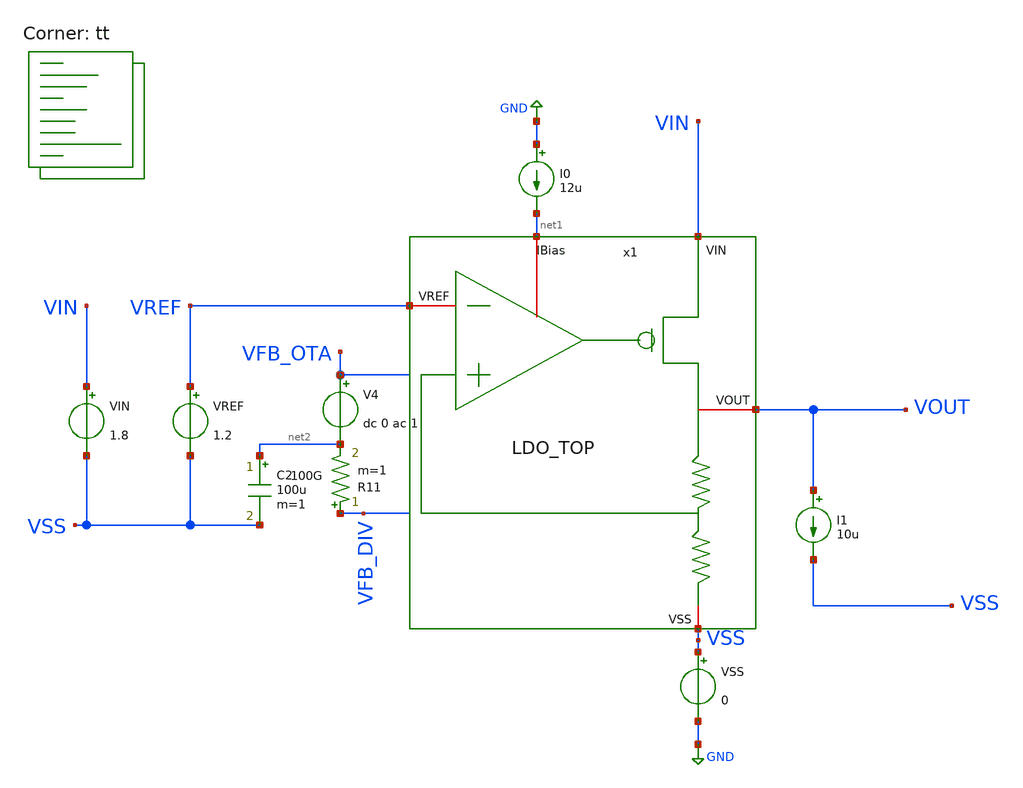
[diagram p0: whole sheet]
** sch_path: LDO_1p5V/tests/stb.sch
**.subckt stb
VSS VSS GND 0
VREF VREF VSS 1.2
VIN VIN VSS 1.8
I0 GND net1 12u
I1 VOUT VSS 10u
V4 VFB_OTA net2 dc 0 ac 1
R11 VFB_DIV net2 100G m=1
C2 net2 VSS 100u m=1
x1 VIN net1 VREF VOUT VSS LDO_TOP
**** begin user architecture code


.options savecurrents
.save all

.control
set filetype=ascii

echo ==============================================
echo ===== LDO STABILITY / LOOP GAIN ANALYSIS =====
echo ==============================================

****************************************************
* CASE 1: ILOAD = 10uA
****************************************************

echo ===== CASE 1: ILOAD = 10uA =====

alter I1 10u

op

echo ===== OPERATING POINT - ILOAD = 10uA =====
print v(VIN)
print v(VOUT)
print v(VREF)
print v(VFB_OTA)
print v(VFB_DIV)
print v(VSS)

echo ===== AC ANALYSIS - ILOAD = 10uA =====
ac dec 200 1 10g

echo ===== LOOP GAIN - ILOAD = 10uA =====

* Fuente de prueba V4: dc 0 ac 1
* La fuente está entre VFB_OTA y VFB_DIV
* La señal de retorno se mide en VFB_DIV

let loopgain_10u = -v(VFB_DIV)
let loopgain_10u_db = db(loopgain_10u)
let loopgain_10u_phase_deg = ph(loopgain_10u)*180/3.141592653589793

meas ac loop_gain_dc_10u find loopgain_10u_db at=1
meas ac unity_freq_10u when loopgain_10u_db=0
meas ac phase_at_unity_10u find loopgain_10u_phase_deg when loopgain_10u_db=0

let phase_margin_10u = 180 + phase_at_unity_10u

echo ===== RESULTS - ILOAD = 10uA =====
print loop_gain_dc_10u
print unity_freq_10u
print phase_at_unity_10u
print phase_margin_10u


****************************************************
* CASE 2: ILOAD = 1mA
****************************************************

echo ===== CASE 2: ILOAD = 1mA =====

alter I1 1m

op

echo ===== OPERATING POINT - ILOAD = 1mA =====
print v(VIN)
print v(VOUT)
print v(VREF)
print v(VFB_OTA)
print v(VFB_DIV)
print v(VSS)

echo ===== AC ANALYSIS - ILOAD = 1mA =====
ac dec 200 1 10g

echo ===== LOOP GAIN - ILOAD = 1mA =====

let loopgain_1m = -v(VFB_DIV)
let loopgain_1m_db = db(loopgain_1m)
let loopgain_1m_phase_deg = ph(loopgain_1m)*180/3.141592653589793

meas ac loop_gain_dc_1m find loopgain_1m_db at=1
meas ac unity_freq_1m when loopgain_1m_db=0
meas ac phase_at_unity_1m find loopgain_1m_phase_deg when loopgain_1m_db=0

let phase_margin_1m = 180 + phase_at_unity_1m

echo ===== RESULTS - ILOAD = 1mA =====
print loop_gain_dc_1m
print unity_freq_1m
print phase_at_unity_1m
print phase_margin_1m


****************************************************
* PLOTS - BOTH LOAD CONDITIONS
****************************************************

echo ===== PLOT LOOP GAIN BOTH LOAD CONDITIONS =====

plot ac1.loopgain_10u_db ac2.loopgain_1m_db xlog

echo ===== PLOT LOOP PHASE BOTH LOAD CONDITIONS =====

plot ac1.loopgain_10u_phase_deg ac2.loopgain_1m_phase_deg xlog


****************************************************
* EXPORT DATA
****************************************************

*wrdata loopgain_10u.csv ac1.frequency ac1.loopgain_10u_db ac1.loopgain_10u_phase_deg
*wrdata loopgain_1m.csv ac2.frequency ac2.loopgain_1m_db ac2.loopgain_1m_phase_deg

.endc


.lib $::SKYWATER_MODELS/sky130.lib.spice tt
**** end user architecture code
**.ends

* expanding   symbol:  /foss/designs/Curso_Semiconductores/LDO_1p5V/schematics/LDO_TOP.sym # of
*+ pins=5
** sym_path: LDO/LDO_TOP.sym
** sch_path: LDO/LDO_TOP.sch
.subckt LDO_TOP VIN IBias VREF VOUT VSS
*.iopin VIN
*.iopin VREF
*.iopin IBias
*.iopin VOUT
*.iopin VSS
x1 VIN IBias VREF VOUT net1 net1 VSS LDO
.ends


* expanding   symbol:  /foss/designs/Curso_Semiconductores/LDO/LDO.sym # of pins=7
** sym_path: LDO/LDO.sym
** sch_path: LDO/LDO.sch
.subckt LDO VIN IBias VREF VOUT VFB1 VFB2 VSS
*.iopin VIN
*.iopin VREF
*.iopin VFB1
*.iopin VSS
*.iopin VFB2
*.iopin VOUT
*.iopin IBias
XM7 VOUT Vgate VIN VIN sky130_fd_pr__pfet_01v8 L=0.15 W=6 nf=1 ad='int((1 + 1)/2) * 6 / 1 * 0.29' as='int((1 + 2)/2) * 6 / 1 * 0.29'
+ pd='2*int((1 + 1)/2) * (6 / 1 + 0.29)' ps='2*int((1 + 2)/2) * (6 / 1 + 0.29)' nrd='0.29 / 6 ' nrs='0.29 / 6 '
+ sa=0 sb=0 sd=0 mult=50 m=50
XC3 Vgate VOUT sky130_fd_pr__model__cap_mim W=10 L=10 MF=1 m=1
x1 VIN Vgate VREF VFB1 IBias VSS OTA_5T
x2 VOUT VFB2 VSS RES_FB
.ends


* expanding   symbol:  /foss/designs/Curso_Semiconductores/OTA_5T/OTA_5T.sym # of pins=6
** sym_path: /foss/designs/Curso_Semiconductores/OTA_5T/OTA_5T.sym
** sch_path: /foss/designs/Curso_Semiconductores/OTA_5T/OTA_5T.sch
.subckt OTA_5T VIN VOUT_AMP VINN VINP IB VSS
*.iopin VIN
*.iopin VSS
*.iopin VOUT_AMP
*.iopin IB
*.iopin VINN
*.iopin VINP
XM1 IB IB VSS VSS sky130_fd_pr__nfet_01v8 L=1 W=2.5 nf=1 ad='int((1 + 1)/2) * 2.5 / 1 * 0.29' as='int((1 + 2)/2) * 2.5 / 1 * 0.29'
+ pd='2*int((1 + 1)/2) * (2.5 / 1 + 0.29)' ps='2*int((1 + 2)/2) * (2.5 / 1 + 0.29)' nrd='0.29 / 2.5 ' nrs='0.29 / 2.5 '
+ sa=0 sb=0 sd=0 mult=4 m=4
XM2 tail IB VSS VSS sky130_fd_pr__nfet_01v8 L=1 W=2.5 nf=1 ad='int((1 + 1)/2) * 2.5 / 1 * 0.29' as='int((1 + 2)/2) * 2.5 / 1 * 0.29'
+ pd='2*int((1 + 1)/2) * (2.5 / 1 + 0.29)' ps='2*int((1 + 2)/2) * (2.5 / 1 + 0.29)' nrd='0.29 / 2.5 ' nrs='0.29 / 2.5 '
+ sa=0 sb=0 sd=0 mult=4 m=4
XM3 net1 VINP tail VSS sky130_fd_pr__nfet_01v8 L=1 W=3 nf=1 ad='int((1 + 1)/2) * 3 / 1 * 0.29' as='int((1 + 2)/2) * 3 / 1 * 0.29'
+ pd='2*int((1 + 1)/2) * (3 / 1 + 0.29)' ps='2*int((1 + 2)/2) * (3 / 1 + 0.29)' nrd='0.29 / 3 ' nrs='0.29 / 3 '
+ sa=0 sb=0 sd=0 mult=4 m=4
XM4 VOUT_AMP VINN tail VSS sky130_fd_pr__nfet_01v8 L=1 W=3 nf=1 ad='int((1 + 1)/2) * 3 / 1 * 0.29' as='int((1 + 2)/2) * 3 / 1 * 0.29'
+ pd='2*int((1 + 1)/2) * (3 / 1 + 0.29)' ps='2*int((1 + 2)/2) * (3 / 1 + 0.29)' nrd='0.29 / 3 ' nrs='0.29 / 3 '
+ sa=0 sb=0 sd=0 mult=4 m=4
XM5 VOUT_AMP net1 VIN VIN sky130_fd_pr__pfet_01v8 L=1 W=6 nf=1 ad='int((1 + 1)/2) * 6 / 1 * 0.29' as='int((1 + 2)/2) * 6 / 1 * 0.29'
+ pd='2*int((1 + 1)/2) * (6 / 1 + 0.29)' ps='2*int((1 + 2)/2) * (6 / 1 + 0.29)' nrd='0.29 / 6 ' nrs='0.29 / 6 '
+ sa=0 sb=0 sd=0 mult=4 m=4
XM6 net1 net1 VIN VIN sky130_fd_pr__pfet_01v8 L=1 W=6 nf=1 ad='int((1 + 1)/2) * 6 / 1 * 0.29' as='int((1 + 2)/2) * 6 / 1 * 0.29'
+ pd='2*int((1 + 1)/2) * (6 / 1 + 0.29)' ps='2*int((1 + 2)/2) * (6 / 1 + 0.29)' nrd='0.29 / 6 ' nrs='0.29 / 6 '
+ sa=0 sb=0 sd=0 mult=4 m=4
XD tail VSS tail VSS sky130_fd_pr__nfet_01v8 L=0.15 W=3 nf=1 ad='int((1 + 1)/2) * 3 / 1 * 0.29' as='int((1 + 2)/2) * 3 / 1 * 0.29'
+ pd='2*int((1 + 1)/2) * (3 / 1 + 0.29)' ps='2*int((1 + 2)/2) * (3 / 1 + 0.29)' nrd='0.29 / 3 ' nrs='0.29 / 3 '
+ sa=0 sb=0 sd=0 mult=4 m=4
XM7 VIN VIN VIN VIN sky130_fd_pr__pfet_01v8 L=0.15 W=6 nf=1 ad='int((1 + 1)/2) * 6 / 1 * 0.29' as='int((1 + 2)/2) * 6 / 1 * 0.29'
+ pd='2*int((1 + 1)/2) * (6 / 1 + 0.29)' ps='2*int((1 + 2)/2) * (6 / 1 + 0.29)' nrd='0.29 / 6 ' nrs='0.29 / 6 '
+ sa=0 sb=0 sd=0 mult=4 m=4
.ends


* expanding   symbol:  /foss/designs/Curso_Semiconductores/RES_FB/RES_FB.sym # of pins=3
** sym_path: RES_FB/RES_FB.sym
** sch_path: RES_FB/RES_FB.sch
.subckt RES_FB VOUT VFB VSS
*.iopin VOUT
*.iopin VFB
*.iopin VSS
XR11 net1 VOUT VSS sky130_fd_pr__res_xhigh_po_0p69 L=8.62 mult=1 m=1
XR1 VFB net1 VSS sky130_fd_pr__res_xhigh_po_0p69 L=8.62 mult=1 m=1
XR2 net8 VFB VSS sky130_fd_pr__res_xhigh_po_0p69 L=8.62 mult=1 m=1
XR3 net4 net8 VSS sky130_fd_pr__res_xhigh_po_0p69 L=8.62 mult=1 m=1
XR4 net2 net4 VSS sky130_fd_pr__res_xhigh_po_0p69 L=8.62 mult=1 m=1
XR5 net5 net2 VSS sky130_fd_pr__res_xhigh_po_0p69 L=8.62 mult=1 m=1
XR6 net3 net5 VSS sky130_fd_pr__res_xhigh_po_0p69 L=8.62 mult=1 m=1
XR7 net7 net3 VSS sky130_fd_pr__res_xhigh_po_0p69 L=8.62 mult=1 m=1
XR8 net6 net7 VSS sky130_fd_pr__res_xhigh_po_0p69 L=8.62 mult=1 m=1
XR9 VSS net6 VSS sky130_fd_pr__res_xhigh_po_0p69 L=8.62 mult=1 m=1
.ends

.GLOBAL GND
.end
